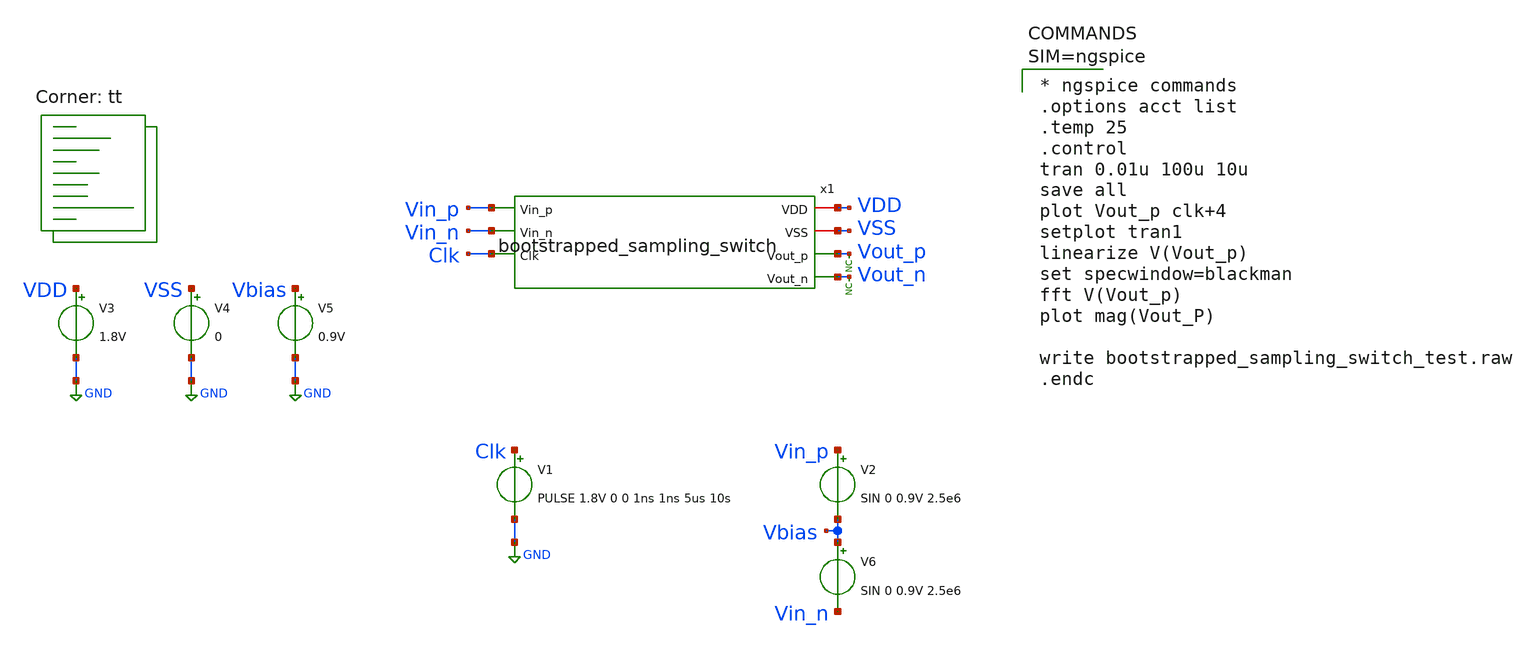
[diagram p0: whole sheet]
** sch_path: xschem/tests/bootstrapped_sampling_switch/bootstrapped_sfdr_test.sch
**.subckt bootstrapped_sfdr_test
V3 VDD GND 1.8V
V4 VSS GND 0
x1 VDD Vin_p VSS Vin_n Clk Vout_p Vout_n bootstrapped_sampling_switch
V1 Clk GND PULSE 1.8V 0 0 1ns 1ns 5us 10s
V2 Vin_p Vbias SIN 0 0.9V 2.5e6
* noconn Vout_p
* noconn Vout_n
V5 Vbias GND 0.9V
V6 Vbias Vin_n SIN 0 0.9V 2.5e6
**** begin user architecture code
 *.lib $::SKYWATER_MODELS/sky130.lib.spice tt
.include $::SKYWATER_STDCELLS/sky130_fd_sc_hd.spice

.lib $::SKYWATER_MODELS/sky130.lib.spice tt


* ngspice commands
.options acct list
.temp 25
.control
tran 0.01u 100u 10u
save all
plot Vout_p clk+4
setplot tran1
linearize V(Vout_p)
set specwindow=blackman
fft V(Vout_p)
plot mag(Vout_P)

write bootstrapped_sampling_switch_test.raw
.endc






**** end user architecture code
**.ends

* expanding   symbol:  src/bootstrapped_sampling_switch/bootstrapped_sampling_switch.sym # of pins=7
** sym_path: xschem/src/bootstrapped_sampling_switch/bootstrapped_sampling_switch.sym
** sch_path: xschem/src/bootstrapped_sampling_switch/bootstrapped_sampling_switch.sch
.subckt bootstrapped_sampling_switch VDD Vin_p VSS Vin_n Clk Vout_p Vout_n
*.iopin VDD
*.ipin Vin_p
*.opin Vout_p
*.iopin VSS
*.opin Vout_n
*.ipin Vin_n
*.ipin Clk
XM1 net3 Clk_n VSS VSS sky130_fd_pr__nfet_01v8 L=0.15 W=0.91 nf=1 ad='int((nf+1)/2) * W/nf * 0.29' as='int((nf+2)/2) * W/nf * 0.29'
+ pd='2*int((nf+1)/2) * (W/nf + 0.29)' ps='2*int((nf+2)/2) * (W/nf + 0.29)' nrd='0.29 / W' nrs='0.29 / W'
+ sa=0 sb=0 sd=0 mult=8 m=8
XM2 net1 Clk VDD VDD sky130_fd_pr__pfet_01v8 L=0.15 W=1.605 nf=1 ad='int((nf+1)/2) * W/nf * 0.29' as='int((nf+2)/2) * W/nf * 0.29'
+ pd='2*int((nf+1)/2) * (W/nf + 0.29)' ps='2*int((nf+2)/2) * (W/nf + 0.29)' nrd='0.29 / W' nrs='0.29 / W'
+ sa=0 sb=0 sd=0 mult=1 m=1
XM3 net1 Clk net3 VSS sky130_fd_pr__nfet_01v8 L=0.15 W=0.91 nf=1 ad='int((nf+1)/2) * W/nf * 0.29' as='int((nf+2)/2) * W/nf * 0.29'
+ pd='2*int((nf+1)/2) * (W/nf + 0.29)' ps='2*int((nf+2)/2) * (W/nf + 0.29)' nrd='0.29 / W' nrs='0.29 / W'
+ sa=0 sb=0 sd=0 mult=1 m=1
XC1 net2 net3 sky130_fd_pr__cap_mim_m3_1 W=30 L=30 MF=1 m=1
XM4 net2 net4 VDD net2 sky130_fd_pr__pfet_01v8 L=0.15 W=5 nf=1 ad='int((nf+1)/2) * W/nf * 0.29' as='int((nf+2)/2) * W/nf * 0.29'
+ pd='2*int((nf+1)/2) * (W/nf + 0.29)' ps='2*int((nf+2)/2) * (W/nf + 0.29)' nrd='0.29 / W' nrs='0.29 / W'
+ sa=0 sb=0 sd=0 mult=1 m=1
XM5 net4 net1 net2 net2 sky130_fd_pr__pfet_01v8 L=0.15 W=1.605 nf=1 ad='int((nf+1)/2) * W/nf * 0.29'
+ as='int((nf+2)/2) * W/nf * 0.29' pd='2*int((nf+1)/2) * (W/nf + 0.29)' ps='2*int((nf+2)/2) * (W/nf + 0.29)'
+ nrd='0.29 / W' nrs='0.29 / W' sa=0 sb=0 sd=0 mult=1 m=1
XM6 net1 net4 net3 VSS sky130_fd_pr__nfet_01v8 L=0.15 W=0.91 nf=1 ad='int((nf+1)/2) * W/nf * 0.29' as='int((nf+2)/2) * W/nf * 0.29'
+ pd='2*int((nf+1)/2) * (W/nf + 0.29)' ps='2*int((nf+2)/2) * (W/nf + 0.29)' nrd='0.29 / W' nrs='0.29 / W'
+ sa=0 sb=0 sd=0 mult=1 m=1
XM7 Vin_p net4 net3 VSS sky130_fd_pr__nfet_01v8 L=0.15 W=0.91 nf=1 ad='int((nf+1)/2) * W/nf * 0.29' as='int((nf+2)/2) * W/nf * 0.29'
+ pd='2*int((nf+1)/2) * (W/nf + 0.29)' ps='2*int((nf+2)/2) * (W/nf + 0.29)' nrd='0.29 / W' nrs='0.29 / W'
+ sa=0 sb=0 sd=0 mult=1 m=1
XM8 Vin_p net4 Vout_p VSS sky130_fd_pr__nfet_01v8 L=0.15 W=0.91 nf=1 ad='int((nf+1)/2) * W/nf * 0.29'
+ as='int((nf+2)/2) * W/nf * 0.29' pd='2*int((nf+1)/2) * (W/nf + 0.29)' ps='2*int((nf+2)/2) * (W/nf + 0.29)'
+ nrd='0.29 / W' nrs='0.29 / W' sa=0 sb=0 sd=0 mult=75 m=75
XM9 net4 VDD net5 VSS sky130_fd_pr__nfet_01v8 L=0.15 W=0.91 nf=1 ad='int((nf+1)/2) * W/nf * 0.29' as='int((nf+2)/2) * W/nf * 0.29'
+ pd='2*int((nf+1)/2) * (W/nf + 0.29)' ps='2*int((nf+2)/2) * (W/nf + 0.29)' nrd='0.29 / W' nrs='0.29 / W'
+ sa=0 sb=0 sd=0 mult=2 m=2
XM10 net5 Clk_n VSS VSS sky130_fd_pr__nfet_01v8 L=0.15 W=0.91 nf=1 ad='int((nf+1)/2) * W/nf * 0.29' as='int((nf+2)/2) * W/nf * 0.29'
+ pd='2*int((nf+1)/2) * (W/nf + 0.29)' ps='2*int((nf+2)/2) * (W/nf + 0.29)' nrd='0.29 / W' nrs='0.29 / W'
+ sa=0 sb=0 sd=0 mult=1 m=1
x1 Clk VSS VSS VDD VDD Clk_n sky130_fd_sc_hd__clkinv_1
XM11 net8 Clk_n VSS VSS sky130_fd_pr__nfet_01v8 L=0.15 W=0.91 nf=1 ad='int((nf+1)/2) * W/nf * 0.29' as='int((nf+2)/2) * W/nf * 0.29'
+ pd='2*int((nf+1)/2) * (W/nf + 0.29)' ps='2*int((nf+2)/2) * (W/nf + 0.29)' nrd='0.29 / W' nrs='0.29 / W'
+ sa=0 sb=0 sd=0 mult=8 m=8
XM12 net6 Clk VDD VDD sky130_fd_pr__pfet_01v8 L=0.15 W=1.605 nf=1 ad='int((nf+1)/2) * W/nf * 0.29' as='int((nf+2)/2) * W/nf * 0.29'
+ pd='2*int((nf+1)/2) * (W/nf + 0.29)' ps='2*int((nf+2)/2) * (W/nf + 0.29)' nrd='0.29 / W' nrs='0.29 / W'
+ sa=0 sb=0 sd=0 mult=1 m=1
XM13 net6 Clk net8 VSS sky130_fd_pr__nfet_01v8 L=0.15 W=0.91 nf=1 ad='int((nf+1)/2) * W/nf * 0.29' as='int((nf+2)/2) * W/nf * 0.29'
+ pd='2*int((nf+1)/2) * (W/nf + 0.29)' ps='2*int((nf+2)/2) * (W/nf + 0.29)' nrd='0.29 / W' nrs='0.29 / W'
+ sa=0 sb=0 sd=0 mult=1 m=1
XC2 net7 net8 sky130_fd_pr__cap_mim_m3_1 W=30 L=30 MF=1 m=1
XM14 net7 net9 VDD net7 sky130_fd_pr__pfet_01v8 L=0.15 W=5 nf=1 ad='int((nf+1)/2) * W/nf * 0.29' as='int((nf+2)/2) * W/nf * 0.29'
+ pd='2*int((nf+1)/2) * (W/nf + 0.29)' ps='2*int((nf+2)/2) * (W/nf + 0.29)' nrd='0.29 / W' nrs='0.29 / W'
+ sa=0 sb=0 sd=0 mult=1 m=1
XM15 net9 net6 net7 net7 sky130_fd_pr__pfet_01v8 L=0.15 W=1.605 nf=1 ad='int((nf+1)/2) * W/nf * 0.29'
+ as='int((nf+2)/2) * W/nf * 0.29' pd='2*int((nf+1)/2) * (W/nf + 0.29)' ps='2*int((nf+2)/2) * (W/nf + 0.29)'
+ nrd='0.29 / W' nrs='0.29 / W' sa=0 sb=0 sd=0 mult=1 m=1
XM16 net6 net9 net8 VSS sky130_fd_pr__nfet_01v8 L=0.15 W=0.91 nf=1 ad='int((nf+1)/2) * W/nf * 0.29' as='int((nf+2)/2) * W/nf * 0.29'
+ pd='2*int((nf+1)/2) * (W/nf + 0.29)' ps='2*int((nf+2)/2) * (W/nf + 0.29)' nrd='0.29 / W' nrs='0.29 / W'
+ sa=0 sb=0 sd=0 mult=1 m=1
XM17 Vin_n net9 net8 VSS sky130_fd_pr__nfet_01v8 L=0.15 W=0.91 nf=1 ad='int((nf+1)/2) * W/nf * 0.29'
+ as='int((nf+2)/2) * W/nf * 0.29' pd='2*int((nf+1)/2) * (W/nf + 0.29)' ps='2*int((nf+2)/2) * (W/nf + 0.29)'
+ nrd='0.29 / W' nrs='0.29 / W' sa=0 sb=0 sd=0 mult=1 m=1
XM18 Vin_n net9 Vout_n VSS sky130_fd_pr__nfet_01v8 L=0.15 W=0.91 nf=1 ad='int((nf+1)/2) * W/nf * 0.29'
+ as='int((nf+2)/2) * W/nf * 0.29' pd='2*int((nf+1)/2) * (W/nf + 0.29)' ps='2*int((nf+2)/2) * (W/nf + 0.29)'
+ nrd='0.29 / W' nrs='0.29 / W' sa=0 sb=0 sd=0 mult=75 m=75
XM19 net9 VDD net10 VSS sky130_fd_pr__nfet_01v8 L=0.15 W=0.91 nf=1 ad='int((nf+1)/2) * W/nf * 0.29' as='int((nf+2)/2) * W/nf * 0.29'
+ pd='2*int((nf+1)/2) * (W/nf + 0.29)' ps='2*int((nf+2)/2) * (W/nf + 0.29)' nrd='0.29 / W' nrs='0.29 / W'
+ sa=0 sb=0 sd=0 mult=2 m=2
XM20 net10 Clk_n VSS VSS sky130_fd_pr__nfet_01v8 L=0.15 W=0.91 nf=1 ad='int((nf+1)/2) * W/nf * 0.29'
+ as='int((nf+2)/2) * W/nf * 0.29' pd='2*int((nf+1)/2) * (W/nf + 0.29)' ps='2*int((nf+2)/2) * (W/nf + 0.29)'
+ nrd='0.29 / W' nrs='0.29 / W' sa=0 sb=0 sd=0 mult=1 m=1
.ends

.GLOBAL GND
.end
